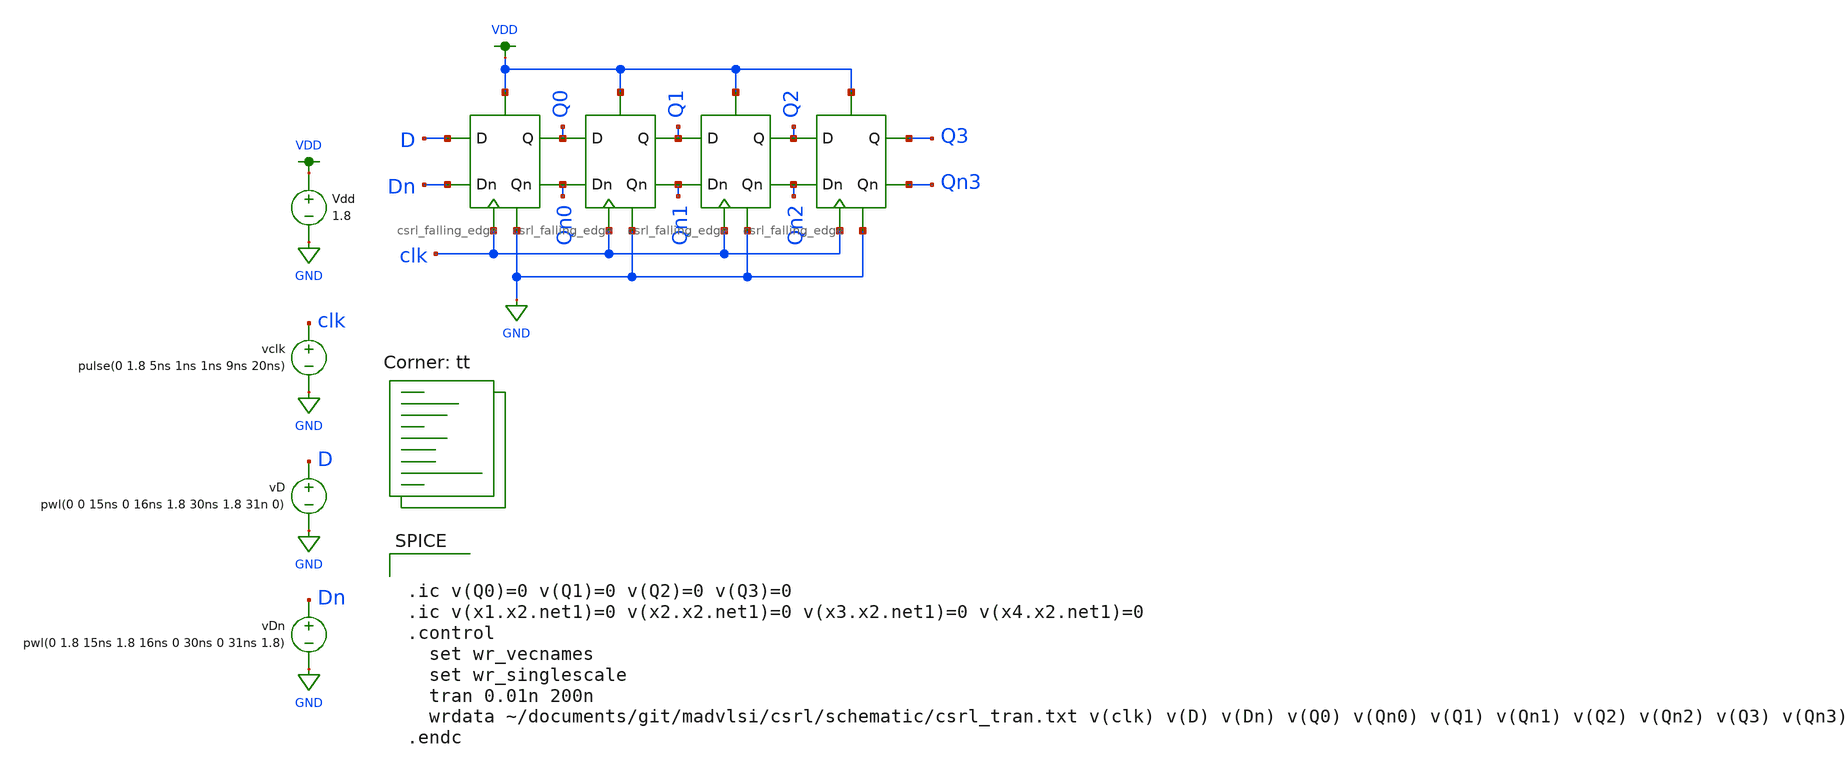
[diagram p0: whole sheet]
** sch_path: csrl/schematic/csrl_falling_edge_x4_tran.sch
**.subckt csrl_falling_edge_x4_tran
Vdd VDD GND 1.8
vclk clk GND pulse(0 1.8 5ns 1ns 1ns 9ns 20ns)
vD D GND pwl(0 0 15ns 0 16ns 1.8 30ns 1.8 31n 0)
vDn Dn GND pwl(0 1.8 15ns 1.8 16ns 0 30ns 0 31ns 1.8)
X1 D Dn Qn0 Q0 GND clk VDD csrl_falling_edge
X2 Q0 Qn0 Qn1 Q1 GND clk VDD csrl_falling_edge
X3 Q1 Qn1 Qn2 Q2 GND clk VDD csrl_falling_edge
X4 Q2 Qn2 Qn3 Q3 GND clk VDD csrl_falling_edge
**** begin user architecture code


.ic v(Q0)=0 v(Q1)=0 v(Q2)=0 v(Q3)=0
.ic v(x1.x2.net1)=0 v(x2.x2.net1)=0 v(x3.x2.net1)=0 v(x4.x2.net1)=0
.control
  set wr_vecnames
  set wr_singlescale
  tran 0.01n 200n
  wrdata ~/documents/git/madvlsi/csrl/schematic/csrl_tran.txt v(clk) v(D) v(Dn) v(Q0) v(Qn0) v(Q1)
+ v(Qn1) v(Q2) v(Qn2) v(Q3) v(Qn3)
.endc

.lib $::SKYWATER_MODELS/sky130.lib.spice tt
**** end user architecture code
**.ends
.GLOBAL GND
.GLOBAL VDD
.end
